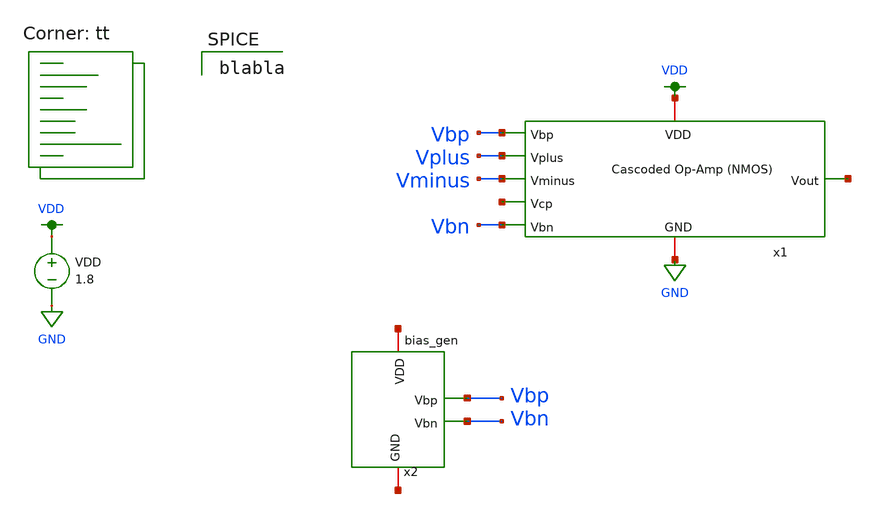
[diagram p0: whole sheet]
** sch_path: final/schematics/cascoded_opamp_tb.sch
**.subckt cascoded_opamp_tb
x1 Vbp Vplus Vminus net1 Vbn VDD GND net2 cascoded_opamp
x2 net3 Vbp Vbn net4 bias_gen
VDD VDD GND 1.8
**** begin user architecture code
.lib $::SKYWATER_MODELS/sky130.lib.spice tt

blabla

**** end user architecture code
**.ends

* expanding   symbol:  cascoded_opamp.sym # of pins=8
** sym_path: final/schematics/cascoded_opamp.sym
** sch_path: final/schematics/cascoded_opamp.sch
.subckt cascoded_opamp Vbp Vplus Vminus Vcp Vbn VDD GND Vout
*.ipin Vbp
*.ipin Vplus
*.ipin Vminus
*.ipin Vcp
*.ipin Vbn
*.iopin VDD
*.iopin GND
*.opin Vout
XM1 net1 Vbn GND GND sky130_fd_pr__nfet_01v8 L=0.15 W=1 nf=1 ad='int((nf+1)/2) * W/nf * 0.29' as='int((nf+2)/2) * W/nf * 0.29'
+ pd='2*int((nf+1)/2) * (W/nf + 0.29)' ps='2*int((nf+2)/2) * (W/nf + 0.29)' nrd='0.29 / W' nrs='0.29 / W'
+ sa=0 sb=0 sd=0 mult=1 m=1
XM2 net2 Vminus net1 GND sky130_fd_pr__nfet_01v8 L=0.15 W=1 nf=1 ad='int((nf+1)/2) * W/nf * 0.29' as='int((nf+2)/2) * W/nf * 0.29'
+ pd='2*int((nf+1)/2) * (W/nf + 0.29)' ps='2*int((nf+2)/2) * (W/nf + 0.29)' nrd='0.29 / W' nrs='0.29 / W'
+ sa=0 sb=0 sd=0 mult=1 m=1
XM3 net1 Vplus net3 GND sky130_fd_pr__nfet_01v8 L=0.15 W=1 nf=1 ad='int((nf+1)/2) * W/nf * 0.29' as='int((nf+2)/2) * W/nf * 0.29'
+ pd='2*int((nf+1)/2) * (W/nf + 0.29)' ps='2*int((nf+2)/2) * (W/nf + 0.29)' nrd='0.29 / W' nrs='0.29 / W'
+ sa=0 sb=0 sd=0 mult=1 m=1
XM4 net2 Vbp VDD VDD sky130_fd_pr__pfet_01v8 L=0.15 W=1 nf=1 ad='int((nf+1)/2) * W/nf * 0.29' as='int((nf+2)/2) * W/nf * 0.29'
+ pd='2*int((nf+1)/2) * (W/nf + 0.29)' ps='2*int((nf+2)/2) * (W/nf + 0.29)' nrd='0.29 / W' nrs='0.29 / W'
+ sa=0 sb=0 sd=0 mult=1 m=1
XM5 net3 Vbp VDD VDD sky130_fd_pr__pfet_01v8 L=0.15 W=1 nf=1 ad='int((nf+1)/2) * W/nf * 0.29' as='int((nf+2)/2) * W/nf * 0.29'
+ pd='2*int((nf+1)/2) * (W/nf + 0.29)' ps='2*int((nf+2)/2) * (W/nf + 0.29)' nrd='0.29 / W' nrs='0.29 / W'
+ sa=0 sb=0 sd=0 mult=1 m=1
XM6 net4 Vcp net2 VDD sky130_fd_pr__pfet_01v8 L=0.15 W=1 nf=1 ad='int((nf+1)/2) * W/nf * 0.29' as='int((nf+2)/2) * W/nf * 0.29'
+ pd='2*int((nf+1)/2) * (W/nf + 0.29)' ps='2*int((nf+2)/2) * (W/nf + 0.29)' nrd='0.29 / W' nrs='0.29 / W'
+ sa=0 sb=0 sd=0 mult=1 m=1
XM7 Vout Vcp net3 VDD sky130_fd_pr__pfet_01v8 L=0.15 W=1 nf=1 ad='int((nf+1)/2) * W/nf * 0.29' as='int((nf+2)/2) * W/nf * 0.29'
+ pd='2*int((nf+1)/2) * (W/nf + 0.29)' ps='2*int((nf+2)/2) * (W/nf + 0.29)' nrd='0.29 / W' nrs='0.29 / W'
+ sa=0 sb=0 sd=0 mult=1 m=1
XM8 GND net4 net4 GND sky130_fd_pr__nfet_01v8 L=0.15 W=1 nf=1 ad='int((nf+1)/2) * W/nf * 0.29' as='int((nf+2)/2) * W/nf * 0.29'
+ pd='2*int((nf+1)/2) * (W/nf + 0.29)' ps='2*int((nf+2)/2) * (W/nf + 0.29)' nrd='0.29 / W' nrs='0.29 / W'
+ sa=0 sb=0 sd=0 mult=1 m=1
XM9 Vout net4 GND GND sky130_fd_pr__nfet_01v8 L=0.15 W=1 nf=1 ad='int((nf+1)/2) * W/nf * 0.29' as='int((nf+2)/2) * W/nf * 0.29'
+ pd='2*int((nf+1)/2) * (W/nf + 0.29)' ps='2*int((nf+2)/2) * (W/nf + 0.29)' nrd='0.29 / W' nrs='0.29 / W'
+ sa=0 sb=0 sd=0 mult=1 m=1
.ends


* expanding   symbol:  /home/madvlsi/Documents/madvlsi/final/schematics/bias_gen/bias_gen.sym # of
*+ pins=4
** sym_path: final/schematics/bias_gen/bias_gen.sym
** sch_path: final/schematics/bias_gen/bias_gen.sch
.subckt bias_gen VDD Vbp Vbn GND
*.iopin VDD
*.opin Vbp
*.iopin GND
*.opin Vbn
**** begin user architecture code

.param len=0.5 wid=3

**** end user architecture code
XM10 net3 net1 net1 GND sky130_fd_pr__nfet_01v8 L={len} W={wid} nf=1 ad='int((nf+1)/2) * W/nf * 0.29'
+ as='int((nf+2)/2) * W/nf * 0.29' pd='2*int((nf+1)/2) * (W/nf + 0.29)' ps='2*int((nf+2)/2) * (W/nf + 0.29)'
+ nrd='0.29 / W' nrs='0.29 / W' sa=0 sb=0 sd=0 mult=10 m=10
XM11 Vbn Vbn GND GND sky130_fd_pr__nfet_01v8 L={len} W={wid} nf=1 ad='int((nf+1)/2) * W/nf * 0.29' as='int((nf+2)/2) * W/nf * 0.29'
+ pd='2*int((nf+1)/2) * (W/nf + 0.29)' ps='2*int((nf+2)/2) * (W/nf + 0.29)' nrd='0.29 / W' nrs='0.29 / W'
+ sa=0 sb=0 sd=0 mult=1 m=1
XM12 GND Vbp GND GND sky130_fd_pr__nfet_01v8 L=10 W=10 nf=1 ad='int((nf+1)/2) * W/nf * 0.29' as='int((nf+2)/2) * W/nf * 0.29'
+ pd='2*int((nf+1)/2) * (W/nf + 0.29)' ps='2*int((nf+2)/2) * (W/nf + 0.29)' nrd='0.29 / W' nrs='0.29 / W'
+ sa=0 sb=0 sd=0 mult=1 m=1
XM13 VDD Vbp net1 VDD sky130_fd_pr__pfet_01v8 L={len} W={wid} nf=1 ad='int((nf+1)/2) * W/nf * 0.29' as='int((nf+2)/2) * W/nf * 0.29'
+ pd='2*int((nf+1)/2) * (W/nf + 0.29)' ps='2*int((nf+2)/2) * (W/nf + 0.29)' nrd='0.29 / W' nrs='0.29 / W'
+ sa=0 sb=0 sd=0 mult=1 m=1
XM14 GND Vbn Vbp GND sky130_fd_pr__nfet_01v8 L={len} W={wid} nf=1 ad='int((nf+1)/2) * W/nf * 0.29' as='int((nf+2)/2) * W/nf * 0.29'
+ pd='2*int((nf+1)/2) * (W/nf + 0.29)' ps='2*int((nf+2)/2) * (W/nf + 0.29)' nrd='0.29 / W' nrs='0.29 / W'
+ sa=0 sb=0 sd=0 mult=1 m=1
XM15 net2 net1 GND GND sky130_fd_pr__nfet_01v8 L={len} W={wid} nf=1 ad='int((nf+1)/2) * W/nf * 0.29'
+ as='int((nf+2)/2) * W/nf * 0.29' pd='2*int((nf+1)/2) * (W/nf + 0.29)' ps='2*int((nf+2)/2) * (W/nf + 0.29)'
+ nrd='0.29 / W' nrs='0.29 / W' sa=0 sb=0 sd=0 mult=1 m=1
XM16 VDD net2 net2 VDD sky130_fd_pr__pfet_01v8 L={len} W={wid} nf=1 ad='int((nf+1)/2) * W/nf * 0.29'
+ as='int((nf+2)/2) * W/nf * 0.29' pd='2*int((nf+1)/2) * (W/nf + 0.29)' ps='2*int((nf+2)/2) * (W/nf + 0.29)'
+ nrd='0.29 / W' nrs='0.29 / W' sa=0 sb=0 sd=0 mult=1 m=1
XM17 Vbp net2 VDD VDD sky130_fd_pr__pfet_01v8 L={len} W={wid} nf=1 ad='int((nf+1)/2) * W/nf * 0.29' as='int((nf+2)/2) * W/nf * 0.29'
+ pd='2*int((nf+1)/2) * (W/nf + 0.29)' ps='2*int((nf+2)/2) * (W/nf + 0.29)' nrd='0.29 / W' nrs='0.29 / W'
+ sa=0 sb=0 sd=0 mult=1 m=1
XM18 Vbn Vbp VDD VDD sky130_fd_pr__pfet_01v8 L={len} W={wid} nf=1 ad='int((nf+1)/2) * W/nf * 0.29' as='int((nf+2)/2) * W/nf * 0.29'
+ pd='2*int((nf+1)/2) * (W/nf + 0.29)' ps='2*int((nf+2)/2) * (W/nf + 0.29)' nrd='0.29 / W' nrs='0.29 / W'
+ sa=0 sb=0 sd=0 mult=1 m=1
XR2 GND net3 GND sky130_fd_pr__res_high_po_0p35 L=9 mult=1 m=1
.ends

.GLOBAL VDD
.GLOBAL GND
.end
